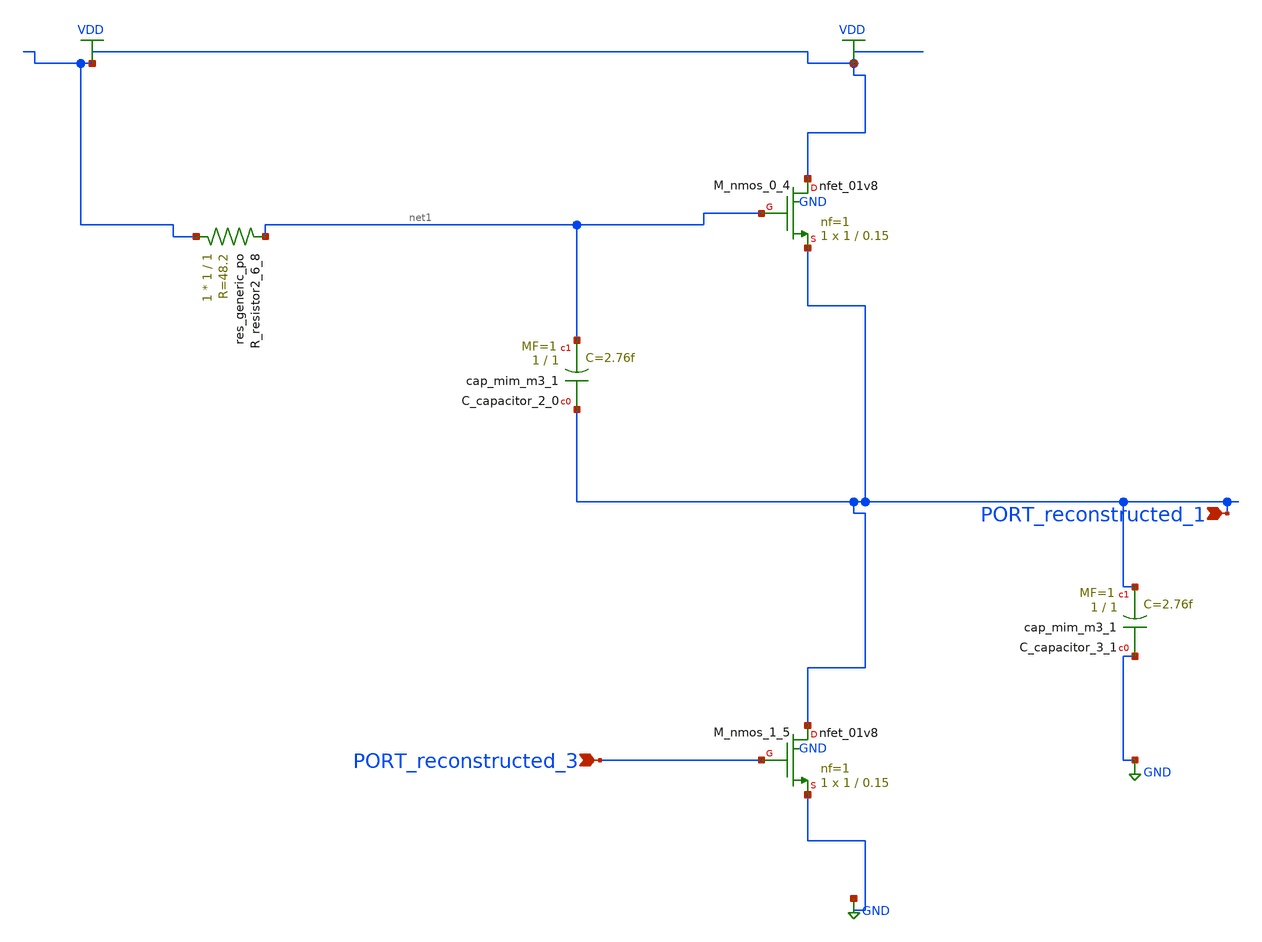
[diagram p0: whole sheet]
** sch_path: schematics/AMSNet/377.sch
**.subckt 377 PORT_reconstructed_1 PORT_reconstructed_3
*.ipin PORT_reconstructed_1
*.ipin PORT_reconstructed_3
XC_capacitor_2_0 PORT_reconstructed_1 net1 sky130_fd_pr__cap_mim_m3_1 W=1 L=1 MF=1 m=1
XC_capacitor_3_1 GND PORT_reconstructed_1 sky130_fd_pr__cap_mim_m3_1 W=1 L=1 MF=1 m=1
XM_nmos_0_4 VDD net1 PORT_reconstructed_1 GND sky130_fd_pr__nfet_01v8 L=0.15 W=1 nf=1 ad='int((1 + 1)/2) * 1 / 1 * 0.29'
+ as='int((1 + 2)/2) * 1 / 1 * 0.29' pd='2*int((1 + 1)/2) * (1 / 1 + 0.29)' ps='2*int((1 + 2)/2) * (1 / 1 + 0.29)'
+ nrd='0.29 / 1 ' nrs='0.29 / 1 ' sa=0 sb=0 sd=0 mult=1 m=1
XM_nmos_1_5 PORT_reconstructed_1 PORT_reconstructed_3 GND GND sky130_fd_pr__nfet_01v8 L=0.15 W=1 nf=1
+ ad='int((1 + 1)/2) * 1 / 1 * 0.29' as='int((1 + 2)/2) * 1 / 1 * 0.29' pd='2*int((1 + 1)/2) * (1 / 1 + 0.29)'
+ ps='2*int((1 + 2)/2) * (1 / 1 + 0.29)' nrd='0.29 / 1 ' nrs='0.29 / 1 ' sa=0 sb=0 sd=0 mult=1 m=1
XR_resistor2_6_8 VDD net1 sky130_fd_pr__res_generic_po W=1 L=1 m=1
**.ends
.GLOBAL GND
.GLOBAL VDD
.end
